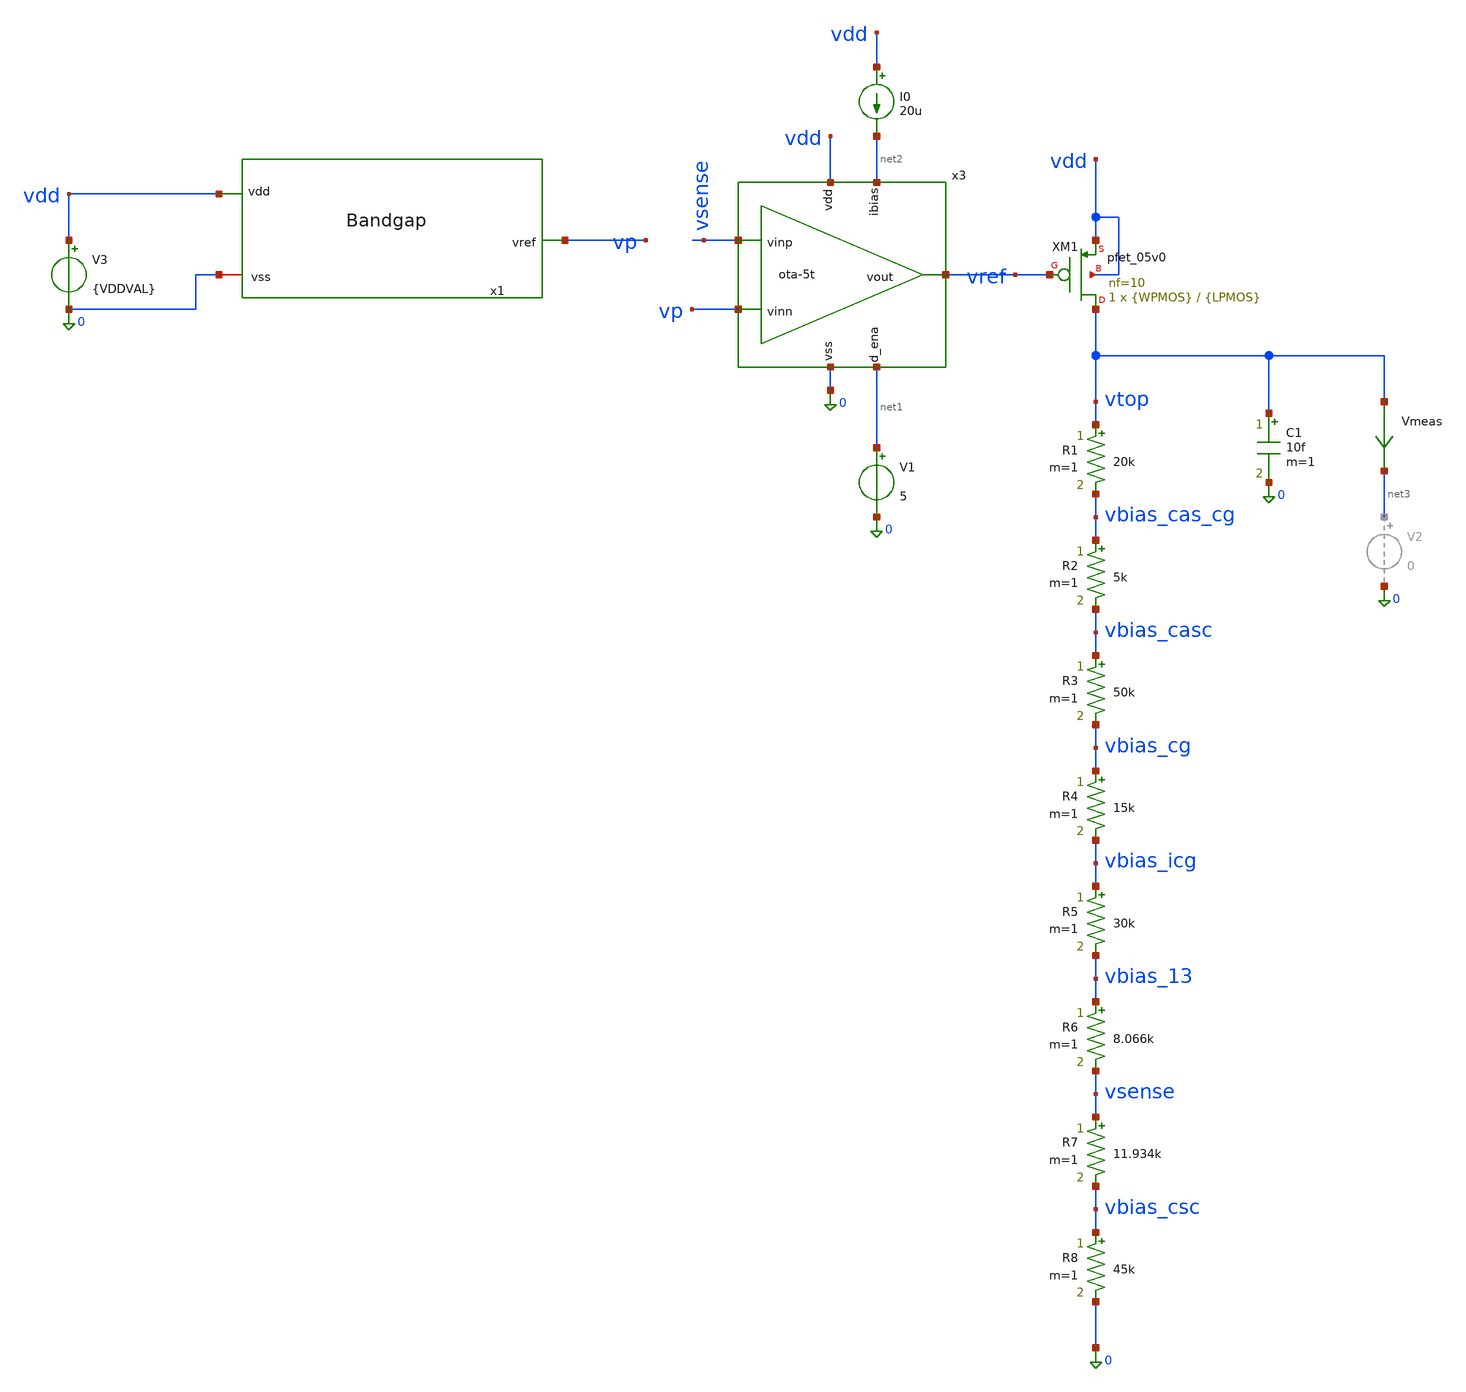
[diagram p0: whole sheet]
** sch_path: xschem/bias_current.sch
**.subckt bias_current
V3 vdd 0 {VDDVAL}
V1 net1 0 5
I0 vdd net2 20u
R1 vtop vbias_cas_cg 20k m=1
R2 vbias_cas_cg vbias_casc 5k m=1
C1 vtop 0 10f m=1
Vmeas vtop net3 0
.save i(vmeas)
x1 vdd vp 0 bandgap
x3 vdd vref vsense vp net2 net1 0 ota-5t
R3 vbias_casc vbias_cg 50k m=1
R4 vbias_cg vbias_icg 15k m=1
R5 vbias_icg vbias_13 30k m=1
R6 vbias_13 vsense 8.066k m=1
R7 vsense vbias_csc 11.934k m=1
R8 vbias_csc 0 45k m=1
XM1 vtop vref vdd vdd pfet_05v0 L={LPMOS} W={WPMOS} nf=10 ad='int((nf+1)/2) * W/nf * 0.18u' as='int((nf+2)/2) * W/nf * 0.18u'
+ pd='2*int((nf+1)/2) * (W/nf + 0.18u)' ps='2*int((nf+2)/2) * (W/nf + 0.18u)' nrd='0.18u / W' nrs='0.18u / W'
+ sa=0 sb=0 sd=0 m=1
**** begin user architecture code


*.option klu
.option method=gear
.option warn=0
.temp 27


.param VDDVAL=5
.param WPMOS=50u
.param LPMOS=2u

.control

* ============================================================
* GF180MCU Bias Current Generator PMOS Sizing / VDD / Temp Sweep
* Corrected for retuned ladder:
*
*   R1 = 20k
*   R2 = 5k
*   R3 = 50k
*   R4 = 15k
*   R5 = 30k
*   R6 = 8.066k
*   R7 = 11.934k
*   R8 = 45k
*
* Important:
*   This block does NOT rely on i(Vmeas).
*   Your current schematic still has Vmeas not in series, so i(Vmeas)
*   is intentionally ignored here.
*
* Output files:
*   bias_current_pmos_sizing_test_report.txt
*   bias_current_pmos_sizing_table.txt
* ============================================================

set noaskquit
set filetype=ascii
set wr_singlescale
set wr_vecnames
set numdgt=10

save all

echo GF180MCU_BIAS_CURRENT_PMOS_SIZING_TEST_REPORT > bias_current_pmos_sizing_test_report.txt
echo ============================================================ >>
+ bias_current_pmos_sizing_test_report.txt
echo . >> bias_current_pmos_sizing_test_report.txt

echo TEST_DESCRIPTION >> bias_current_pmos_sizing_test_report.txt
echo ------------------------------------------------------------ >>
+ bias_current_pmos_sizing_test_report.txt
echo PMOS sizing, VDD, and temperature sweep for the retuned bias-current ladder. >>
+ bias_current_pmos_sizing_test_report.txt
echo This corrected block uses R6=8.066k and R7=11.934k in all current calculations. >>
+ bias_current_pmos_sizing_test_report.txt
echo It does not use i(Vmeas), because Vmeas is not currently in series with XM1. >>
+ bias_current_pmos_sizing_test_report.txt
echo . >> bias_current_pmos_sizing_test_report.txt

echo LADDER_VALUES >> bias_current_pmos_sizing_test_report.txt
echo ------------------------------------------------------------ >>
+ bias_current_pmos_sizing_test_report.txt
echo R1_VTOP_TO_VBIAS_CAS_CG_OHM 20k >> bias_current_pmos_sizing_test_report.txt
echo R2_VBIAS_CAS_CG_TO_VBIAS_CASC_OHM 5k >> bias_current_pmos_sizing_test_report.txt
echo R3_VBIAS_CASC_TO_VBIAS_CG_OHM 50k >> bias_current_pmos_sizing_test_report.txt
echo R4_VBIAS_CG_TO_VBIAS_ICG_OHM 15k >> bias_current_pmos_sizing_test_report.txt
echo R5_VBIAS_ICG_TO_VBIAS_13_OHM 30k >> bias_current_pmos_sizing_test_report.txt
echo R6_VBIAS_13_TO_VSENSE_OHM 8.066k >> bias_current_pmos_sizing_test_report.txt
echo R7_VSENSE_TO_VBIAS_CSC_OHM 11.934k >> bias_current_pmos_sizing_test_report.txt
echo R8_VBIAS_CSC_TO_GND_OHM 45k >> bias_current_pmos_sizing_test_report.txt
echo . >> bias_current_pmos_sizing_test_report.txt

echo TEST_LIMITS >> bias_current_pmos_sizing_test_report.txt
echo ------------------------------------------------------------ >>
+ bias_current_pmos_sizing_test_report.txt
echo TARGET_I_LADDER_A 20u >> bias_current_pmos_sizing_test_report.txt
echo TARGET_VTOP_V 3.7 >> bias_current_pmos_sizing_test_report.txt
echo MAX_ABS_I_ERROR_A 1u >> bias_current_pmos_sizing_test_report.txt
echo MAX_ABS_VTOP_ERROR_V 30m >> bias_current_pmos_sizing_test_report.txt
echo MAX_ABS_VSENSE_ERROR_V 5m >> bias_current_pmos_sizing_test_report.txt
echo MIN_PMOS_SAT_MARGIN_V 0.2 >> bias_current_pmos_sizing_test_report.txt
echo MIN_PMOS_GATE_V 0.2 >> bias_current_pmos_sizing_test_report.txt
echo MAX_PMOS_GATE_MARGIN_FROM_VDD_V 0.2 >> bias_current_pmos_sizing_test_report.txt
echo NOTE_PASS_IF_ALL_MARGIN_COLUMNS_ARE_POSITIVE >> bias_current_pmos_sizing_test_report.txt
echo . >> bias_current_pmos_sizing_test_report.txt

echo TEST_NAME WPMOS LPMOS TEMP_C VDD_V VBG_V VSENSE_V ERR_VBG_MINUS_VSENSE_V VTOP_V VBIAS_CAS_CG_V
+ VBIAS_CASC_V VBIAS_CG_V VBIAS_ICG_V VBIAS_13_V VBIAS_CSC_V I_R1_A I_R2_A I_R3_A I_R4_A I_R5_A I_R6_A I_R7_A
+ I_R8_A I_LADDER_A I_LADDER_ERR_A I_LADDER_ERR_PCT PMOS_GATE_V PMOS_ID_A PMOS_GM_S PMOS_GMBS_S PMOS_GDS_S
+ PMOS_GMID PMOS_VGS PMOS_VDS PMOS_VBS PMOS_VTH PMOS_VOV_ABS PMOS_VDSAT PMOS_SAT_MARGIN PMOS_RO PMOS_GMRO
+ IDD_TOTAL_A PDC_UW MARGIN_I_A MARGIN_VTOP_V MARGIN_VSENSE_V MARGIN_SAT_V MARGIN_GATE_LOW_V MARGIN_GATE_HIGH_V >
+ bias_current_pmos_sizing_table.txt

* ============================================================
* Sweep
* ============================================================

foreach lval 1u 2u
  foreach wval 20u 30u 40u 50u 70u 100u
    foreach vddtest 4.5 5.0 5.5
      foreach temptest -40 27 125

        alterparam VDDVAL = $vddtest
        alterparam WPMOS = $wval
        alterparam LPMOS = $lval

        reset
        set temp = $temptest
        save all
        op

        * ------------------------------------------------------------
        * Constants, recreated after reset
        * ------------------------------------------------------------

        let target_i_ladder = 20u
        let target_vtop = 3.7

        let limit_i_err = 1u
        let limit_vtop_err = 30m
        let limit_vsense_err = 5m
        let limit_sat_margin = 0.2
        let limit_gate_low = 0.2
        let limit_gate_high_margin = 0.2

        * ------------------------------------------------------------
        * Node voltages
        * ------------------------------------------------------------

        let v_vdd = v(vdd)
        let v_pgate = v(vref)
        let v_vbg = v(vp)
        let v_vtop = v(vtop)

        let v_vbias_cas_cg = v(vbias_cas_cg)
        let v_vbias_casc = v(vbias_casc)
        let v_vbias_cg = v(vbias_cg)
        let v_vbias_icg = v(vbias_icg)
        let v_vbias_13 = v(vbias_13)
        let v_vsense = v(vsense)
        let v_vbias_csc = v(vbias_csc)

        let err_vbg_vsense = v(vp)-v(vsense)
        let abs_err_vsense = abs(err_vbg_vsense)

        let err_vtop = v(vtop)-target_vtop
        let abs_err_vtop = abs(err_vtop)

        * ------------------------------------------------------------
        * Correct ladder currents
        *
        * These values match the actual retuned schematic:
        *   R6 = 8.066k
        *   R7 = 11.934k
        * ------------------------------------------------------------

        let i_r1 = (v(vtop)-v(vbias_cas_cg))/20k
        let i_r2 = (v(vbias_cas_cg)-v(vbias_casc))/5k
        let i_r3 = (v(vbias_casc)-v(vbias_cg))/50k
        let i_r4 = (v(vbias_cg)-v(vbias_icg))/15k
        let i_r5 = (v(vbias_icg)-v(vbias_13))/30k
        let i_r6 = (v(vbias_13)-v(vsense))/8.066k
        let i_r7 = (v(vsense)-v(vbias_csc))/11.934k
        let i_r8 = v(vbias_csc)/45k

        let i_ladder_avg = (i_r1+i_r2+i_r3+i_r4+i_r5+i_r6+i_r7+i_r8)/8
        let i_ladder_err = i_ladder_avg-target_i_ladder
        let abs_i_ladder_err = abs(i_ladder_err)
        let i_ladder_err_pct = 100*i_ladder_err/target_i_ladder

        * ------------------------------------------------------------
        * PMOS operating point for XM1
        * ------------------------------------------------------------

        let id_xm1 = abs(@m.xm1.m0[id])
        let gm_xm1 = @m.xm1.m0[gm]
        let gmb_xm1 = @m.xm1.m0[gmbs]
        let gds_xm1 = @m.xm1.m0[gds]
        let vgs_xm1 = @m.xm1.m0[vgs]
        let vds_xm1 = @m.xm1.m0[vds]
        let vbs_xm1 = @m.xm1.m0[vbs]
        let vth_xm1 = @m.xm1.m0[vth]
        let vdsat_xm1 = abs(@m.xm1.m0[vdsat])

        let vov_xm1 = abs(vgs_xm1)-abs(vth_xm1)
        let sat_xm1 = abs(vds_xm1)-vdsat_xm1
        let gmid_xm1 = gm_xm1/(id_xm1+1e-30)
        let ro_xm1 = 1/(gds_xm1+1e-30)
        let gmro_xm1 = gm_xm1*ro_xm1

        * ------------------------------------------------------------
        * Supply power
        * ------------------------------------------------------------

        let idd_total = -i(v3)
        let pdc_w = v(vdd)*idd_total
        let pdc_uw = 1e6*pdc_w

        * ------------------------------------------------------------
        * Pass/fail margins
        *
        * Positive margin = pass.
        * Negative margin = fail.
        * No < or > operators are used.
        * ------------------------------------------------------------

        let gate_high_limit = v(vdd)-limit_gate_high_margin

        let margin_i = limit_i_err-abs_i_ladder_err
        let margin_vtop = limit_vtop_err-abs_err_vtop
        let margin_vsense = limit_vsense_err-abs_err_vsense
        let margin_sat = sat_xm1-limit_sat_margin
        let margin_gate_low = v(vref)-limit_gate_low
        let margin_gate_high = gate_high_limit-v(vref)

        * ------------------------------------------------------------
        * Detailed report
        * ------------------------------------------------------------

        echo CASE PMOS_SIZE_VDD_TEMP_SWEEP W $wval L $lval TEMP_C $temptest VDD $vddtest >>
+ bias_current_pmos_sizing_test_report.txt
        echo ------------------------------------------------------------ >>
+ bias_current_pmos_sizing_test_report.txt

        echo NODE_VOLTAGES >> bias_current_pmos_sizing_test_report.txt
        echo VDD_V $&v_vdd >> bias_current_pmos_sizing_test_report.txt
        echo VBG_V $&v_vbg >> bias_current_pmos_sizing_test_report.txt
        echo VSENSE_V $&v_vsense >> bias_current_pmos_sizing_test_report.txt
        echo ERR_VBG_MINUS_VSENSE_V $&err_vbg_vsense >> bias_current_pmos_sizing_test_report.txt
        echo VTOP_V $&v_vtop >> bias_current_pmos_sizing_test_report.txt
        echo VBIAS_CAS_CG_V $&v_vbias_cas_cg >> bias_current_pmos_sizing_test_report.txt
        echo VBIAS_CASC_V $&v_vbias_casc >> bias_current_pmos_sizing_test_report.txt
        echo VBIAS_CG_V $&v_vbias_cg >> bias_current_pmos_sizing_test_report.txt
        echo VBIAS_ICG_V $&v_vbias_icg >> bias_current_pmos_sizing_test_report.txt
        echo VBIAS_13_V $&v_vbias_13 >> bias_current_pmos_sizing_test_report.txt
        echo VSENSE_V $&v_vsense >> bias_current_pmos_sizing_test_report.txt
        echo VBIAS_CSC_V $&v_vbias_csc >> bias_current_pmos_sizing_test_report.txt

        echo LADDER_CURRENTS >> bias_current_pmos_sizing_test_report.txt
        echo I_R1_A $&i_r1 >> bias_current_pmos_sizing_test_report.txt
        echo I_R2_A $&i_r2 >> bias_current_pmos_sizing_test_report.txt
        echo I_R3_A $&i_r3 >> bias_current_pmos_sizing_test_report.txt
        echo I_R4_A $&i_r4 >> bias_current_pmos_sizing_test_report.txt
        echo I_R5_A $&i_r5 >> bias_current_pmos_sizing_test_report.txt
        echo I_R6_A $&i_r6 >> bias_current_pmos_sizing_test_report.txt
        echo I_R7_A $&i_r7 >> bias_current_pmos_sizing_test_report.txt
        echo I_R8_A $&i_r8 >> bias_current_pmos_sizing_test_report.txt
        echo I_LADDER_AVG_A $&i_ladder_avg >> bias_current_pmos_sizing_test_report.txt
        echo I_LADDER_ERR_A $&i_ladder_err >> bias_current_pmos_sizing_test_report.txt
        echo I_LADDER_ERR_PCT $&i_ladder_err_pct >> bias_current_pmos_sizing_test_report.txt

        echo PMOS_OPERATING_POINT >> bias_current_pmos_sizing_test_report.txt
        echo PMOS_GATE_V $&v_pgate >> bias_current_pmos_sizing_test_report.txt
        echo PMOS_ID_A $&id_xm1 >> bias_current_pmos_sizing_test_report.txt
        echo PMOS_GM_S $&gm_xm1 >> bias_current_pmos_sizing_test_report.txt
        echo PMOS_GMBS_S $&gmb_xm1 >> bias_current_pmos_sizing_test_report.txt
        echo PMOS_GDS_S $&gds_xm1 >> bias_current_pmos_sizing_test_report.txt
        echo PMOS_VGS_V $&vgs_xm1 >> bias_current_pmos_sizing_test_report.txt
        echo PMOS_VDS_V $&vds_xm1 >> bias_current_pmos_sizing_test_report.txt
        echo PMOS_VBS_V $&vbs_xm1 >> bias_current_pmos_sizing_test_report.txt
        echo PMOS_VTH_V $&vth_xm1 >> bias_current_pmos_sizing_test_report.txt
        echo PMOS_VOV_ABS_V $&vov_xm1 >> bias_current_pmos_sizing_test_report.txt
        echo PMOS_VDSAT_ABS_V $&vdsat_xm1 >> bias_current_pmos_sizing_test_report.txt
        echo PMOS_SAT_MARGIN_V $&sat_xm1 >> bias_current_pmos_sizing_test_report.txt
        echo PMOS_GMID_1_PER_V $&gmid_xm1 >> bias_current_pmos_sizing_test_report.txt
        echo PMOS_RO_OHM $&ro_xm1 >> bias_current_pmos_sizing_test_report.txt
        echo PMOS_GMRO $&gmro_xm1 >> bias_current_pmos_sizing_test_report.txt

        echo SUPPLY_POWER >> bias_current_pmos_sizing_test_report.txt
        echo IDD_TOTAL_A $&idd_total >> bias_current_pmos_sizing_test_report.txt
        echo PDC_UW $&pdc_uw >> bias_current_pmos_sizing_test_report.txt

        echo PASS_FAIL_MARGINS >> bias_current_pmos_sizing_test_report.txt
        echo NOTE_POSITIVE_MARGIN_MEANS_PASS >> bias_current_pmos_sizing_test_report.txt
        echo MARGIN_I_A $&margin_i >> bias_current_pmos_sizing_test_report.txt
        echo MARGIN_VTOP_V $&margin_vtop >> bias_current_pmos_sizing_test_report.txt
        echo MARGIN_VSENSE_V $&margin_vsense >> bias_current_pmos_sizing_test_report.txt
        echo MARGIN_SAT_V $&margin_sat >> bias_current_pmos_sizing_test_report.txt
        echo MARGIN_GATE_LOW_V $&margin_gate_low >> bias_current_pmos_sizing_test_report.txt
        echo MARGIN_GATE_HIGH_V $&margin_gate_high >> bias_current_pmos_sizing_test_report.txt
        echo . >> bias_current_pmos_sizing_test_report.txt

        * ------------------------------------------------------------
        * Compact table
        * ------------------------------------------------------------

        echo PMOS_SWEEP $wval $lval $temptest $&v_vdd $&v_vbg $&v_vsense $&err_vbg_vsense $&v_vtop
+ $&v_vbias_cas_cg $&v_vbias_casc $&v_vbias_cg $&v_vbias_icg $&v_vbias_13 $&v_vbias_csc $&i_r1 $&i_r2 $&i_r3 $&i_r4
+ $&i_r5 $&i_r6 $&i_r7 $&i_r8 $&i_ladder_avg $&i_ladder_err $&i_ladder_err_pct $&v_pgate $&id_xm1 $&gm_xm1
+ $&gmb_xm1 $&gds_xm1 $&gmid_xm1 $&vgs_xm1 $&vds_xm1 $&vbs_xm1 $&vth_xm1 $&vov_xm1 $&vdsat_xm1 $&sat_xm1
+ $&ro_xm1 $&gmro_xm1 $&idd_total $&pdc_uw $&margin_i $&margin_vtop $&margin_vsense $&margin_sat
+ $&margin_gate_low $&margin_gate_high >> bias_current_pmos_sizing_table.txt

      end
    end
  end
end

echo FILES_WRITTEN >> bias_current_pmos_sizing_test_report.txt
echo ------------------------------------------------------------ >>
+ bias_current_pmos_sizing_test_report.txt
echo bias_current_pmos_sizing_test_report.txt >> bias_current_pmos_sizing_test_report.txt
echo bias_current_pmos_sizing_table.txt >> bias_current_pmos_sizing_test_report.txt
echo . >> bias_current_pmos_sizing_test_report.txt

echo INTERPRETATION_GUIDE >> bias_current_pmos_sizing_test_report.txt
echo ------------------------------------------------------------ >>
+ bias_current_pmos_sizing_test_report.txt
echo Positive margin columns indicate pass for that metric. >>
+ bias_current_pmos_sizing_test_report.txt
echo MARGIN_I_A checks absolute average ladder-current error against 1uA. >>
+ bias_current_pmos_sizing_test_report.txt
echo MARGIN_VTOP_V checks absolute VTOP error against 30mV. >>
+ bias_current_pmos_sizing_test_report.txt
echo MARGIN_VSENSE_V checks absolute VP-minus-VSENSE error against 5mV. >>
+ bias_current_pmos_sizing_test_report.txt
echo MARGIN_SAT_V checks PMOS saturation margin beyond the required 0.2V. >>
+ bias_current_pmos_sizing_test_report.txt
echo This report ignores i(Vmeas); use resistor currents and XM1 device current instead. >>
+ bias_current_pmos_sizing_test_report.txt
echo . >> bias_current_pmos_sizing_test_report.txt

echo ============================================================ >>
+ bias_current_pmos_sizing_test_report.txt
echo END_OF_PMOS_SIZING_TEST_REPORT >> bias_current_pmos_sizing_test_report.txt
echo ============================================================ >>
+ bias_current_pmos_sizing_test_report.txt

.endc




.include ${::180MCU_MODELS}/design.ngspice

.lib ${::180MCU_MODELS}/sm141064.ngspice typical

.lib ${::180MCU_MODELS}/sm141064.ngspice res_typical
.lib ${::180MCU_MODELS}/sm141064.ngspice moscap_typical
.lib ${::180MCU_MODELS}/sm141064.ngspice diode_typical
.lib ${::180MCU_MODELS}/sm141064.ngspice bjt_typical

.lib /home/arjun/eda/pdks/gf180mcuD/libs.tech/ngspice/sm141064.ngspice mimcap_typical
.include /home/arjun/eda/pdks/gf180mcuD/libs.ref/gf180mcu_fd_io/spice/gf180mcu_fd_io.spice
*.include /home/arjun/eda/projects/The-Silent-Owl-GF180MCU-WB-LNA/analog_pad_sp_paramerters/spice_files/extracted_gf180mcu_fd_io__asig_5p0.spice

**** end user architecture code
**.ends
.end
